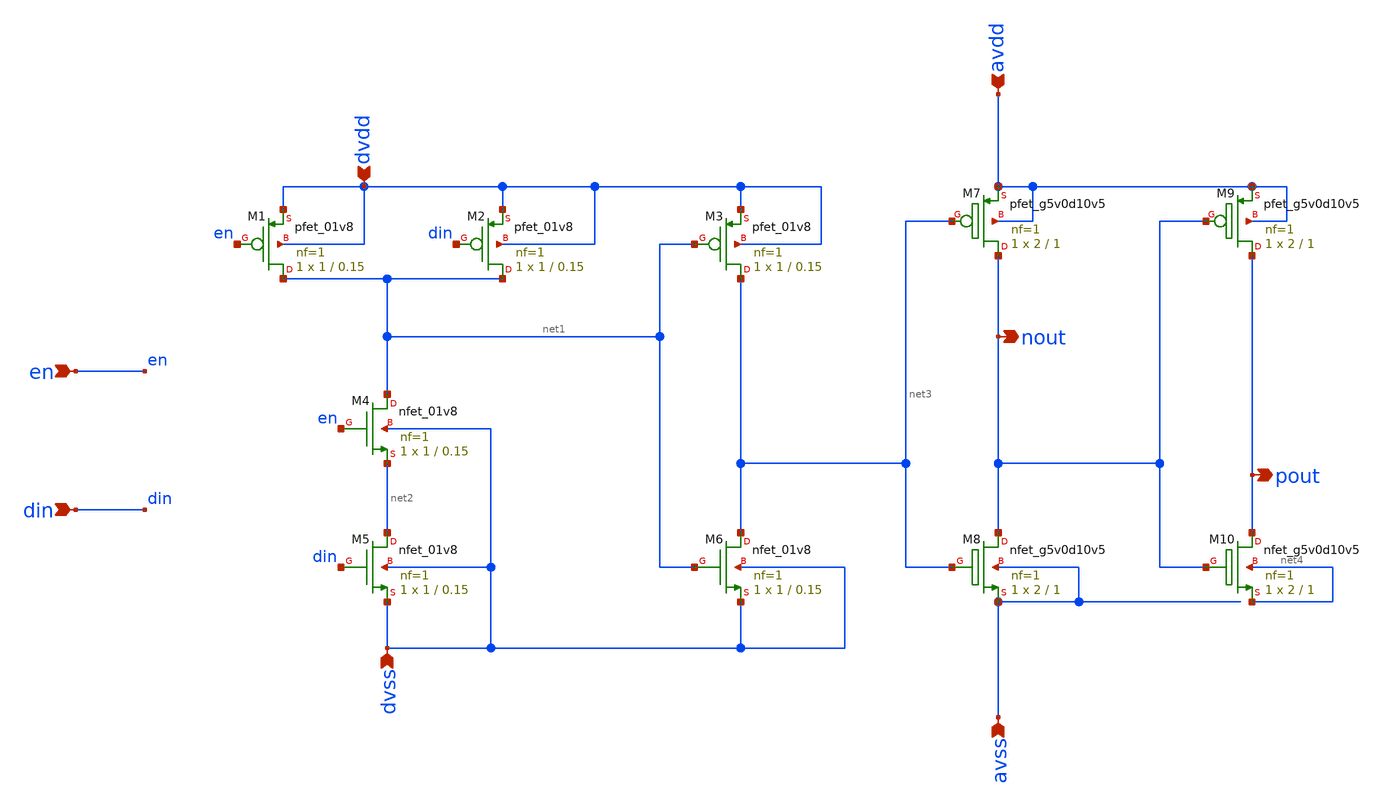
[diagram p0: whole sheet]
** sch_path: xschem/double_output_buffer.sch
**.subckt double_output_buffer din dvdd dvss pout nout en avdd avss
*.ipin din
*.ipin dvdd
*.ipin dvss
*.opin pout
*.opin nout
*.ipin en
*.ipin avdd
*.ipin avss
XM1 net1 en dvdd dvdd sky130_fd_pr__pfet_01v8 L=0.15 W=1 nf=1 ad='int((nf+1)/2) * W/nf * 0.29' as='int((nf+2)/2) * W/nf * 0.29'
+ pd='2*int((nf+1)/2) * (W/nf + 0.29)' ps='2*int((nf+2)/2) * (W/nf + 0.29)' nrd='0.29 / W' nrs='0.29 / W'
+ sa=0 sb=0 sd=0 mult=1 m=1
XM2 net1 din dvdd dvdd sky130_fd_pr__pfet_01v8 L=0.15 W=1 nf=1 ad='int((nf+1)/2) * W/nf * 0.29' as='int((nf+2)/2) * W/nf * 0.29'
+ pd='2*int((nf+1)/2) * (W/nf + 0.29)' ps='2*int((nf+2)/2) * (W/nf + 0.29)' nrd='0.29 / W' nrs='0.29 / W'
+ sa=0 sb=0 sd=0 mult=1 m=1
XM3 net3 net1 dvdd dvdd sky130_fd_pr__pfet_01v8 L=0.15 W=1 nf=1 ad='int((nf+1)/2) * W/nf * 0.29' as='int((nf+2)/2) * W/nf * 0.29'
+ pd='2*int((nf+1)/2) * (W/nf + 0.29)' ps='2*int((nf+2)/2) * (W/nf + 0.29)' nrd='0.29 / W' nrs='0.29 / W'
+ sa=0 sb=0 sd=0 mult=1 m=1
XM4 net1 en net2 dvss sky130_fd_pr__nfet_01v8 L=0.15 W=1 nf=1 ad='int((nf+1)/2) * W/nf * 0.29' as='int((nf+2)/2) * W/nf * 0.29'
+ pd='2*int((nf+1)/2) * (W/nf + 0.29)' ps='2*int((nf+2)/2) * (W/nf + 0.29)' nrd='0.29 / W' nrs='0.29 / W'
+ sa=0 sb=0 sd=0 mult=1 m=1
XM5 net2 din dvss dvss sky130_fd_pr__nfet_01v8 L=0.15 W=1 nf=1 ad='int((nf+1)/2) * W/nf * 0.29' as='int((nf+2)/2) * W/nf * 0.29'
+ pd='2*int((nf+1)/2) * (W/nf + 0.29)' ps='2*int((nf+2)/2) * (W/nf + 0.29)' nrd='0.29 / W' nrs='0.29 / W'
+ sa=0 sb=0 sd=0 mult=1 m=1
XM6 net3 net1 dvss dvss sky130_fd_pr__nfet_01v8 L=0.15 W=1 nf=1 ad='int((nf+1)/2) * W/nf * 0.29' as='int((nf+2)/2) * W/nf * 0.29'
+ pd='2*int((nf+1)/2) * (W/nf + 0.29)' ps='2*int((nf+2)/2) * (W/nf + 0.29)' nrd='0.29 / W' nrs='0.29 / W'
+ sa=0 sb=0 sd=0 mult=1 m=1
XM7 nout net3 avdd avdd sky130_fd_pr__pfet_g5v0d10v5 L=1 W=2 nf=1 ad='int((nf+1)/2) * W/nf * 0.29' as='int((nf+2)/2) * W/nf * 0.29'
+ pd='2*int((nf+1)/2) * (W/nf + 0.29)' ps='2*int((nf+2)/2) * (W/nf + 0.29)' nrd='0.29 / W' nrs='0.29 / W'
+ sa=0 sb=0 sd=0 mult=1 m=1
XM8 nout net3 avss avss sky130_fd_pr__nfet_g5v0d10v5 L=1 W=2 nf=1 ad='int((nf+1)/2) * W/nf * 0.29' as='int((nf+2)/2) * W/nf * 0.29'
+ pd='2*int((nf+1)/2) * (W/nf + 0.29)' ps='2*int((nf+2)/2) * (W/nf + 0.29)' nrd='0.29 / W' nrs='0.29 / W'
+ sa=0 sb=0 sd=0 mult=1 m=1
XM9 pout nout avdd avdd sky130_fd_pr__pfet_g5v0d10v5 L=1 W=2 nf=1 ad='int((nf+1)/2) * W/nf * 0.29' as='int((nf+2)/2) * W/nf * 0.29'
+ pd='2*int((nf+1)/2) * (W/nf + 0.29)' ps='2*int((nf+2)/2) * (W/nf + 0.29)' nrd='0.29 / W' nrs='0.29 / W'
+ sa=0 sb=0 sd=0 mult=1 m=1
XM10 pout nout net4 net4 sky130_fd_pr__nfet_g5v0d10v5 L=1 W=2 nf=1 ad='int((nf+1)/2) * W/nf * 0.29' as='int((nf+2)/2) * W/nf * 0.29'
+ pd='2*int((nf+1)/2) * (W/nf + 0.29)' ps='2*int((nf+2)/2) * (W/nf + 0.29)' nrd='0.29 / W' nrs='0.29 / W'
+ sa=0 sb=0 sd=0 mult=1 m=1
**.ends
.end
